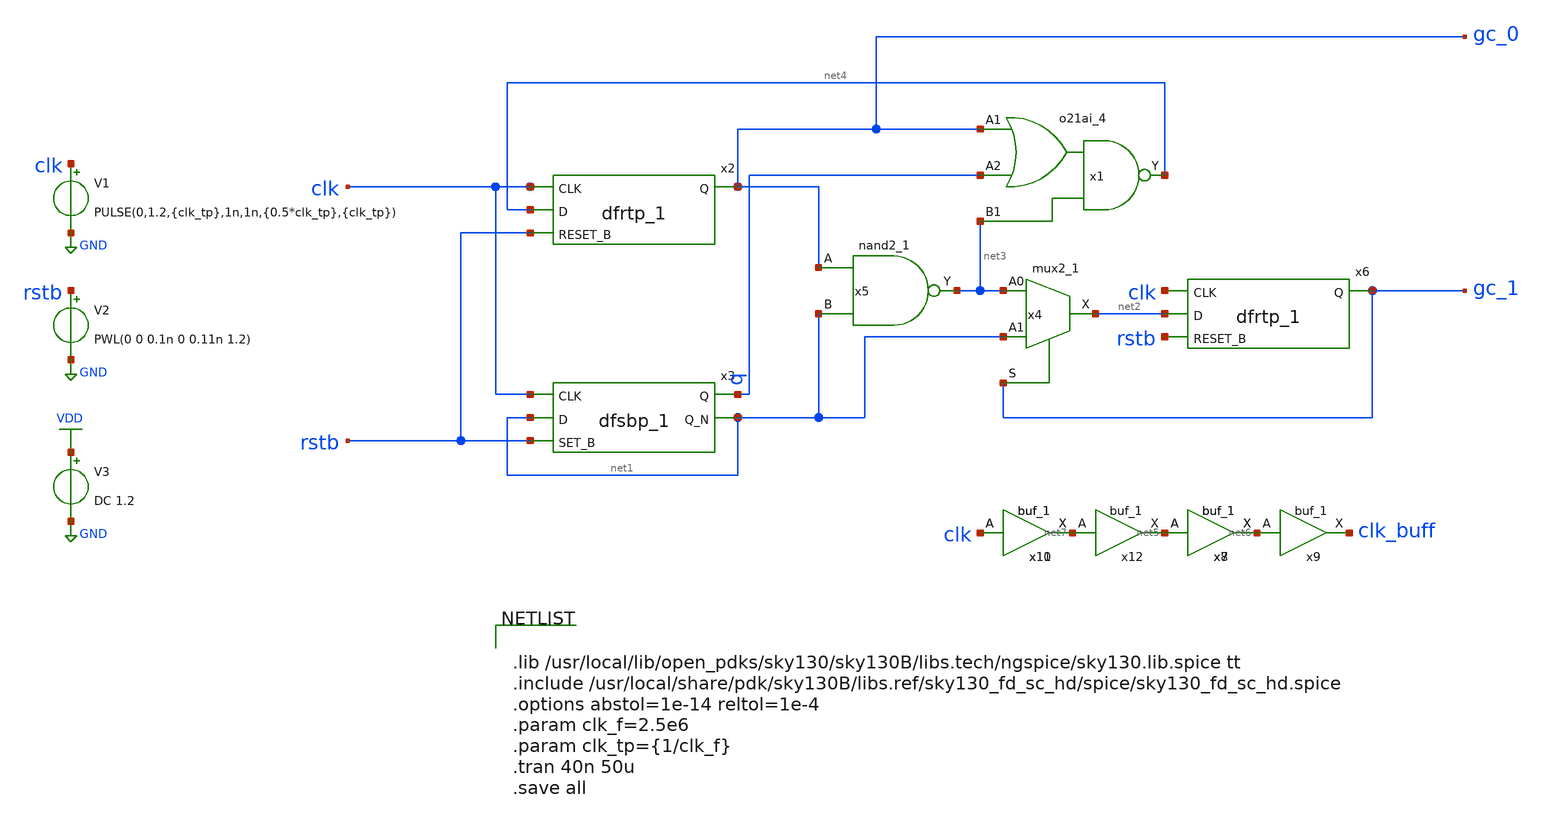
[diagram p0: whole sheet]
** sch_path: xschem/archive/gray_2bit.sch
**.subckt gray_2bit
x1 gc_0 q net3 GND GND VDD VDD net4 sky130_fd_sc_hd__o21ai_4
x2 clk net4 rstb GND GND VDD VDD gc_0 sky130_fd_sc_hd__dfrtp_1
x4 net3 net1 gc_1 GND GND VDD VDD net2 sky130_fd_sc_hd__mux2_1
x5 gc_0 net1 GND GND VDD VDD net3 sky130_fd_sc_hd__nand2_1
x3 clk net1 rstb GND GND VDD VDD q net1 sky130_fd_sc_hd__dfsbp_1
x6 clk net2 rstb GND GND VDD VDD gc_1 sky130_fd_sc_hd__dfrtp_1
V1 clk GND PULSE(0,1.2,{clk_tp},1n,1n,{0.5*clk_tp},{clk_tp})
V2 rstb GND PWL(0 0 0.1n 0 0.11n 1.2)
V3 VDD GND DC 1.2
x7 net5 GND GND VDD VDD net6 sky130_fd_sc_hd__buf_1
x8 net5 GND GND VDD VDD net6 sky130_fd_sc_hd__buf_1
x9 net6 GND GND VDD VDD clk_buff sky130_fd_sc_hd__buf_1
x10 clk GND GND VDD VDD net7 sky130_fd_sc_hd__buf_1
x11 clk GND GND VDD VDD net7 sky130_fd_sc_hd__buf_1
x12 net7 GND GND VDD VDD net5 sky130_fd_sc_hd__buf_1
**** begin user architecture code


.lib /usr/local/lib/open_pdks/sky130/sky130B/libs.tech/ngspice/sky130.lib.spice tt
.include /usr/local/share/pdk/sky130B/libs.ref/sky130_fd_sc_hd/spice/sky130_fd_sc_hd.spice
.options abstol=1e-14 reltol=1e-4
.param clk_f=2.5e6
.param clk_tp={1/clk_f}
.tran 40n 50u
.save all

**** end user architecture code
**.ends
.GLOBAL VDD
.GLOBAL GND
.end
